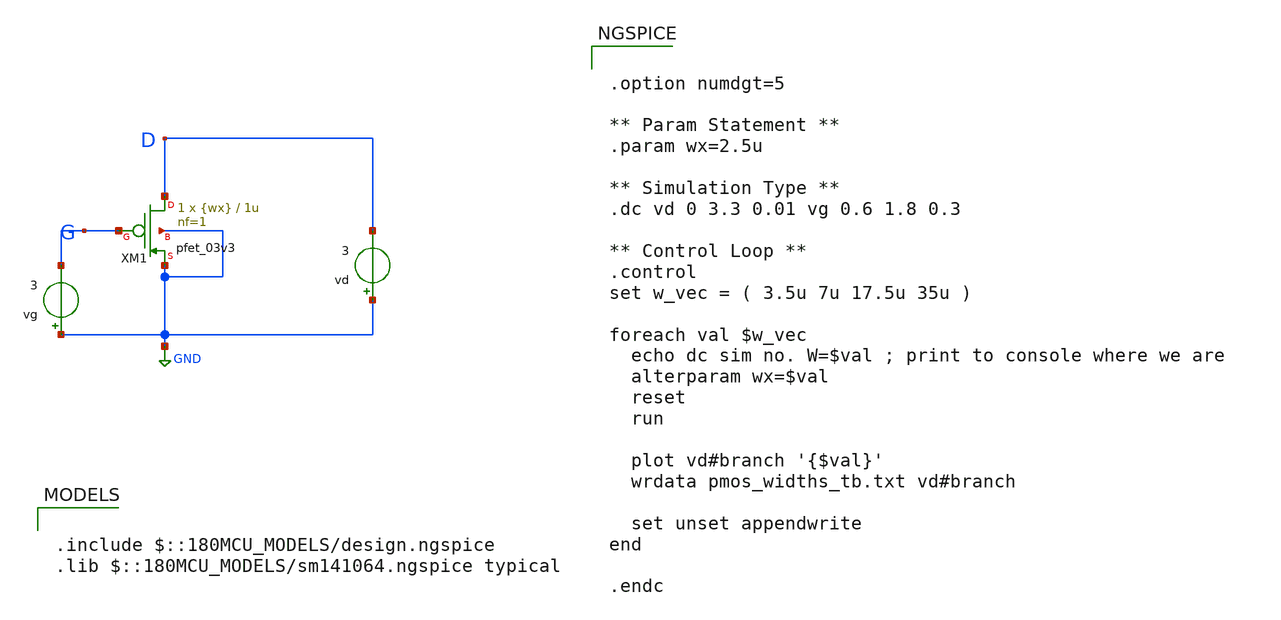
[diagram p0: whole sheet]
** sch_path: designs/switch_matrix_gf180mcu_9t5v0-main/designs/libs/tb_analog/unit_transistors/pmos_widths_tb.sch
**.subckt pmos_widths_tb
vd GND D 3
vg GND G 3
XM1 D G GND GND pfet_03v3 L=1u W={wx} nf=1 ad='int((nf+1)/2) * W/nf * 0.18u' as='int((nf+2)/2) * W/nf * 0.18u'
+ pd='2*int((nf+1)/2) * (W/nf + 0.18u)' ps='2*int((nf+2)/2) * (W/nf + 0.18u)' nrd='0.18u / W' nrs='0.18u / W'
+ sa=0 sb=0 sd=0 m=1
**** begin user architecture code

.include $::180MCU_MODELS/design.ngspice
.lib $::180MCU_MODELS/sm141064.ngspice typical



.option numdgt=5

** Param Statement **
.param wx=2.5u

** Simulation Type **
.dc vd 0 3.3 0.01 vg 0.6 1.8 0.3

** Control Loop **
.control
set w_vec = ( 3.5u 7u 17.5u 35u )

foreach val $w_vec
  echo dc sim no. W=$val ; print to console where we are
  alterparam wx=$val
  reset
  run

  plot vd#branch '{$val}'
  wrdata pmos_widths_tb.txt vd#branch

  set unset appendwrite
end

.endc


**** end user architecture code
**.ends
.GLOBAL GND
.end
